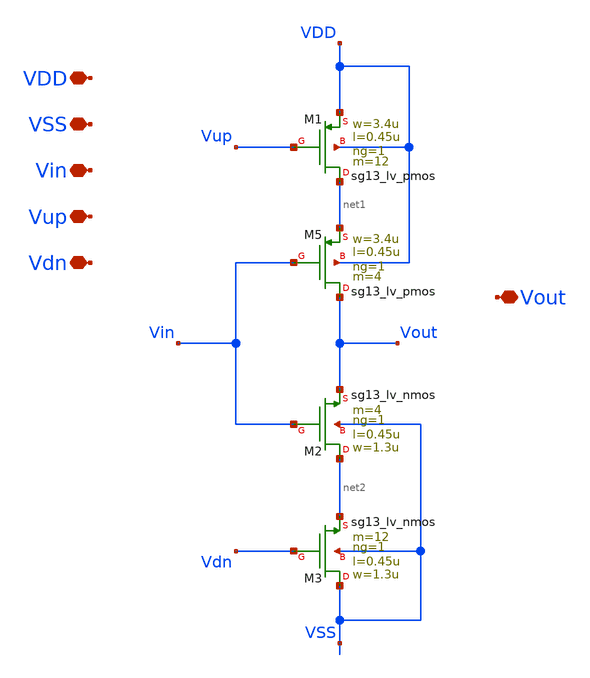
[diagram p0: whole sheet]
** sch_path: unic_cass_wrapper_user_project/ROs_reliability/tristate_inv.sch
**.subckt tristate_inv VDD VSS Vin Vout Vup Vdn
*.iopin VDD
*.iopin VSS
*.iopin Vin
*.iopin Vout
*.iopin Vup
*.iopin Vdn
XM5 Vout Vin net1 VDD sg13_lv_pmos w=3.4u l=0.45u ng=1 m=4 mm_ok=1
XM2 net2 Vin Vout VSS sg13_lv_nmos w=1.3u l=0.45u ng=1 m=4 mm_ok=1
XM1 net1 Vup VDD VDD sg13_lv_pmos w=3.4u l=0.45u ng=1 m=12 mm_ok=1
XM3 VSS Vdn net2 VSS sg13_lv_nmos w=1.3u l=0.45u ng=1 m=12 mm_ok=1
**.ends
.end
